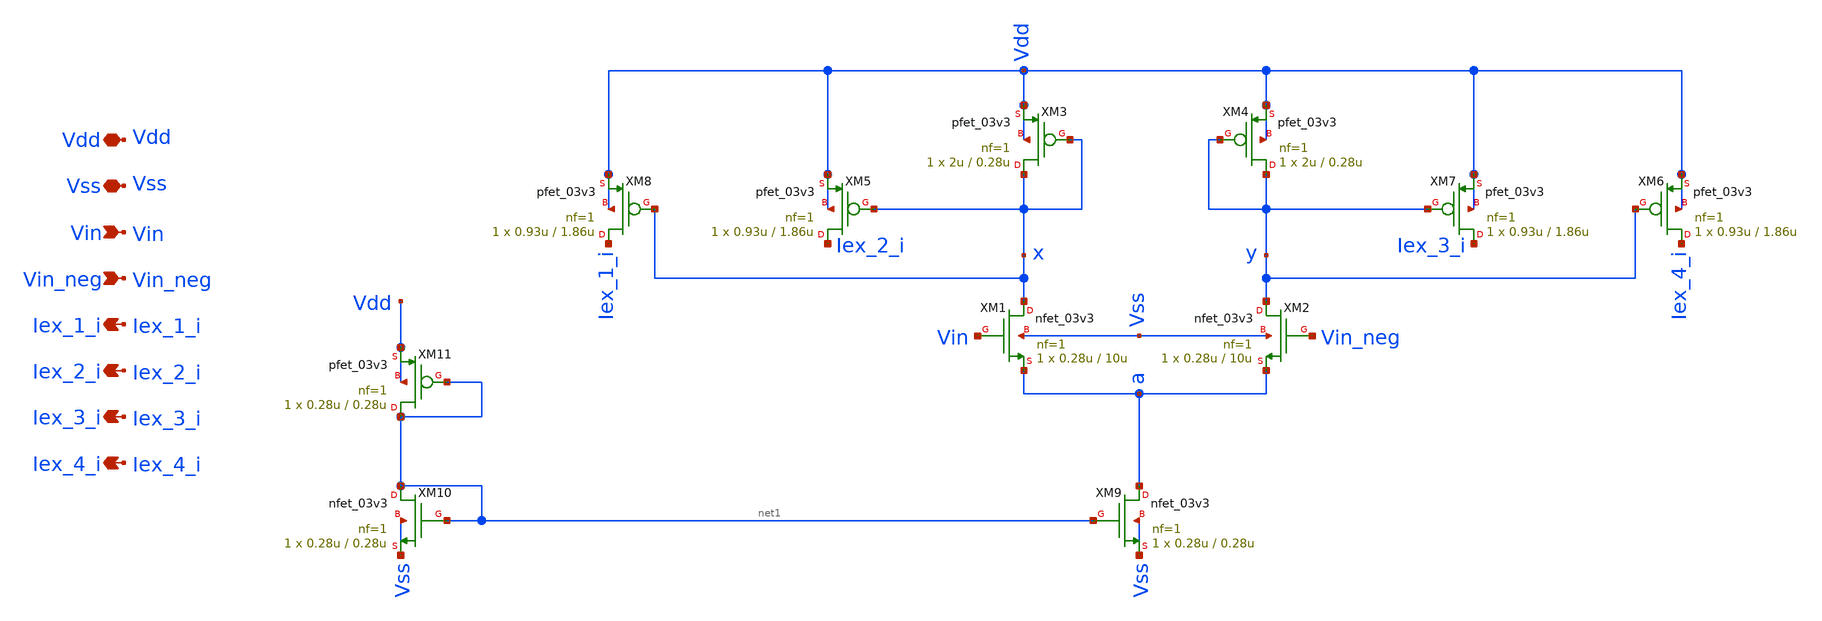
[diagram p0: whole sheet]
** sch_path: sch/encoder/encoder.sch
**.subckt encoder Vdd Vss Vin Vin_neg Iex_1_i Iex_4_i Iex_2_i Iex_3_i
*.iopin Vdd
*.iopin Vss
*.ipin Vin
*.ipin Vin_neg
*.opin Iex_1_i
*.opin Iex_4_i
*.opin Iex_2_i
*.opin Iex_3_i
XM1 x Vin a Vss nfet_03v3 L=10u W=0.28u nf=1 ad='int((nf+1)/2) * W/nf * 0.18u' as='int((nf+2)/2) * W/nf * 0.18u'
+ pd='2*int((nf+1)/2) * (W/nf + 0.18u)' ps='2*int((nf+2)/2) * (W/nf + 0.18u)' nrd='0.18u / W' nrs='0.18u / W'
+ sa=0 sb=0 sd=0 m=1
XM2 y Vin_neg a Vss nfet_03v3 L=10u W=0.28u nf=1 ad='int((nf+1)/2) * W/nf * 0.18u' as='int((nf+2)/2) * W/nf * 0.18u'
+ pd='2*int((nf+1)/2) * (W/nf + 0.18u)' ps='2*int((nf+2)/2) * (W/nf + 0.18u)' nrd='0.18u / W' nrs='0.18u / W'
+ sa=0 sb=0 sd=0 m=1
XM3 x x Vdd Vdd pfet_03v3 L=0.28u W=2u nf=1 ad='int((nf+1)/2) * W/nf * 0.18u' as='int((nf+2)/2) * W/nf * 0.18u'
+ pd='2*int((nf+1)/2) * (W/nf + 0.18u)' ps='2*int((nf+2)/2) * (W/nf + 0.18u)' nrd='0.18u / W' nrs='0.18u / W'
+ sa=0 sb=0 sd=0 m=1
XM4 y y Vdd Vdd pfet_03v3 L=0.28u W=2u nf=1 ad='int((nf+1)/2) * W/nf * 0.18u' as='int((nf+2)/2) * W/nf * 0.18u'
+ pd='2*int((nf+1)/2) * (W/nf + 0.18u)' ps='2*int((nf+2)/2) * (W/nf + 0.18u)' nrd='0.18u / W' nrs='0.18u / W'
+ sa=0 sb=0 sd=0 m=1
XM5 Iex_2_i x Vdd Vdd pfet_03v3 L=1.86u W=0.93u nf=1 ad='int((nf+1)/2) * W/nf * 0.18u' as='int((nf+2)/2) * W/nf * 0.18u'
+ pd='2*int((nf+1)/2) * (W/nf + 0.18u)' ps='2*int((nf+2)/2) * (W/nf + 0.18u)' nrd='0.18u / W' nrs='0.18u / W'
+ sa=0 sb=0 sd=0 m=1
XM7 Iex_3_i y Vdd Vdd pfet_03v3 L=1.86u W=0.93u nf=1 ad='int((nf+1)/2) * W/nf * 0.18u' as='int((nf+2)/2) * W/nf * 0.18u'
+ pd='2*int((nf+1)/2) * (W/nf + 0.18u)' ps='2*int((nf+2)/2) * (W/nf + 0.18u)' nrd='0.18u / W' nrs='0.18u / W'
+ sa=0 sb=0 sd=0 m=1
XM9 a net1 Vss Vss nfet_03v3 L=0.28u W=0.28u nf=1 ad='int((nf+1)/2) * W/nf * 0.18u' as='int((nf+2)/2) * W/nf * 0.18u'
+ pd='2*int((nf+1)/2) * (W/nf + 0.18u)' ps='2*int((nf+2)/2) * (W/nf + 0.18u)' nrd='0.18u / W' nrs='0.18u / W'
+ sa=0 sb=0 sd=0 m=1
XM10 net1 net1 Vss Vss nfet_03v3 L=0.28u W=0.28u nf=1 ad='int((nf+1)/2) * W/nf * 0.18u' as='int((nf+2)/2) * W/nf * 0.18u'
+ pd='2*int((nf+1)/2) * (W/nf + 0.18u)' ps='2*int((nf+2)/2) * (W/nf + 0.18u)' nrd='0.18u / W' nrs='0.18u / W'
+ sa=0 sb=0 sd=0 m=1
XM11 net1 net1 Vdd Vdd pfet_03v3 L=0.28u W=0.28u nf=1 ad='int((nf+1)/2) * W/nf * 0.18u' as='int((nf+2)/2) * W/nf * 0.18u'
+ pd='2*int((nf+1)/2) * (W/nf + 0.18u)' ps='2*int((nf+2)/2) * (W/nf + 0.18u)' nrd='0.18u / W' nrs='0.18u / W'
+ sa=0 sb=0 sd=0 m=1
XM6 Iex_4_i y Vdd Vdd pfet_03v3 L=1.86u W=0.93u nf=1 ad='int((nf+1)/2) * W/nf * 0.18u' as='int((nf+2)/2) * W/nf * 0.18u'
+ pd='2*int((nf+1)/2) * (W/nf + 0.18u)' ps='2*int((nf+2)/2) * (W/nf + 0.18u)' nrd='0.18u / W' nrs='0.18u / W'
+ sa=0 sb=0 sd=0 m=1
XM8 Iex_1_i x Vdd Vdd pfet_03v3 L=1.86u W=0.93u nf=1 ad='int((nf+1)/2) * W/nf * 0.18u' as='int((nf+2)/2) * W/nf * 0.18u'
+ pd='2*int((nf+1)/2) * (W/nf + 0.18u)' ps='2*int((nf+2)/2) * (W/nf + 0.18u)' nrd='0.18u / W' nrs='0.18u / W'
+ sa=0 sb=0 sd=0 m=1
**.ends
.end
